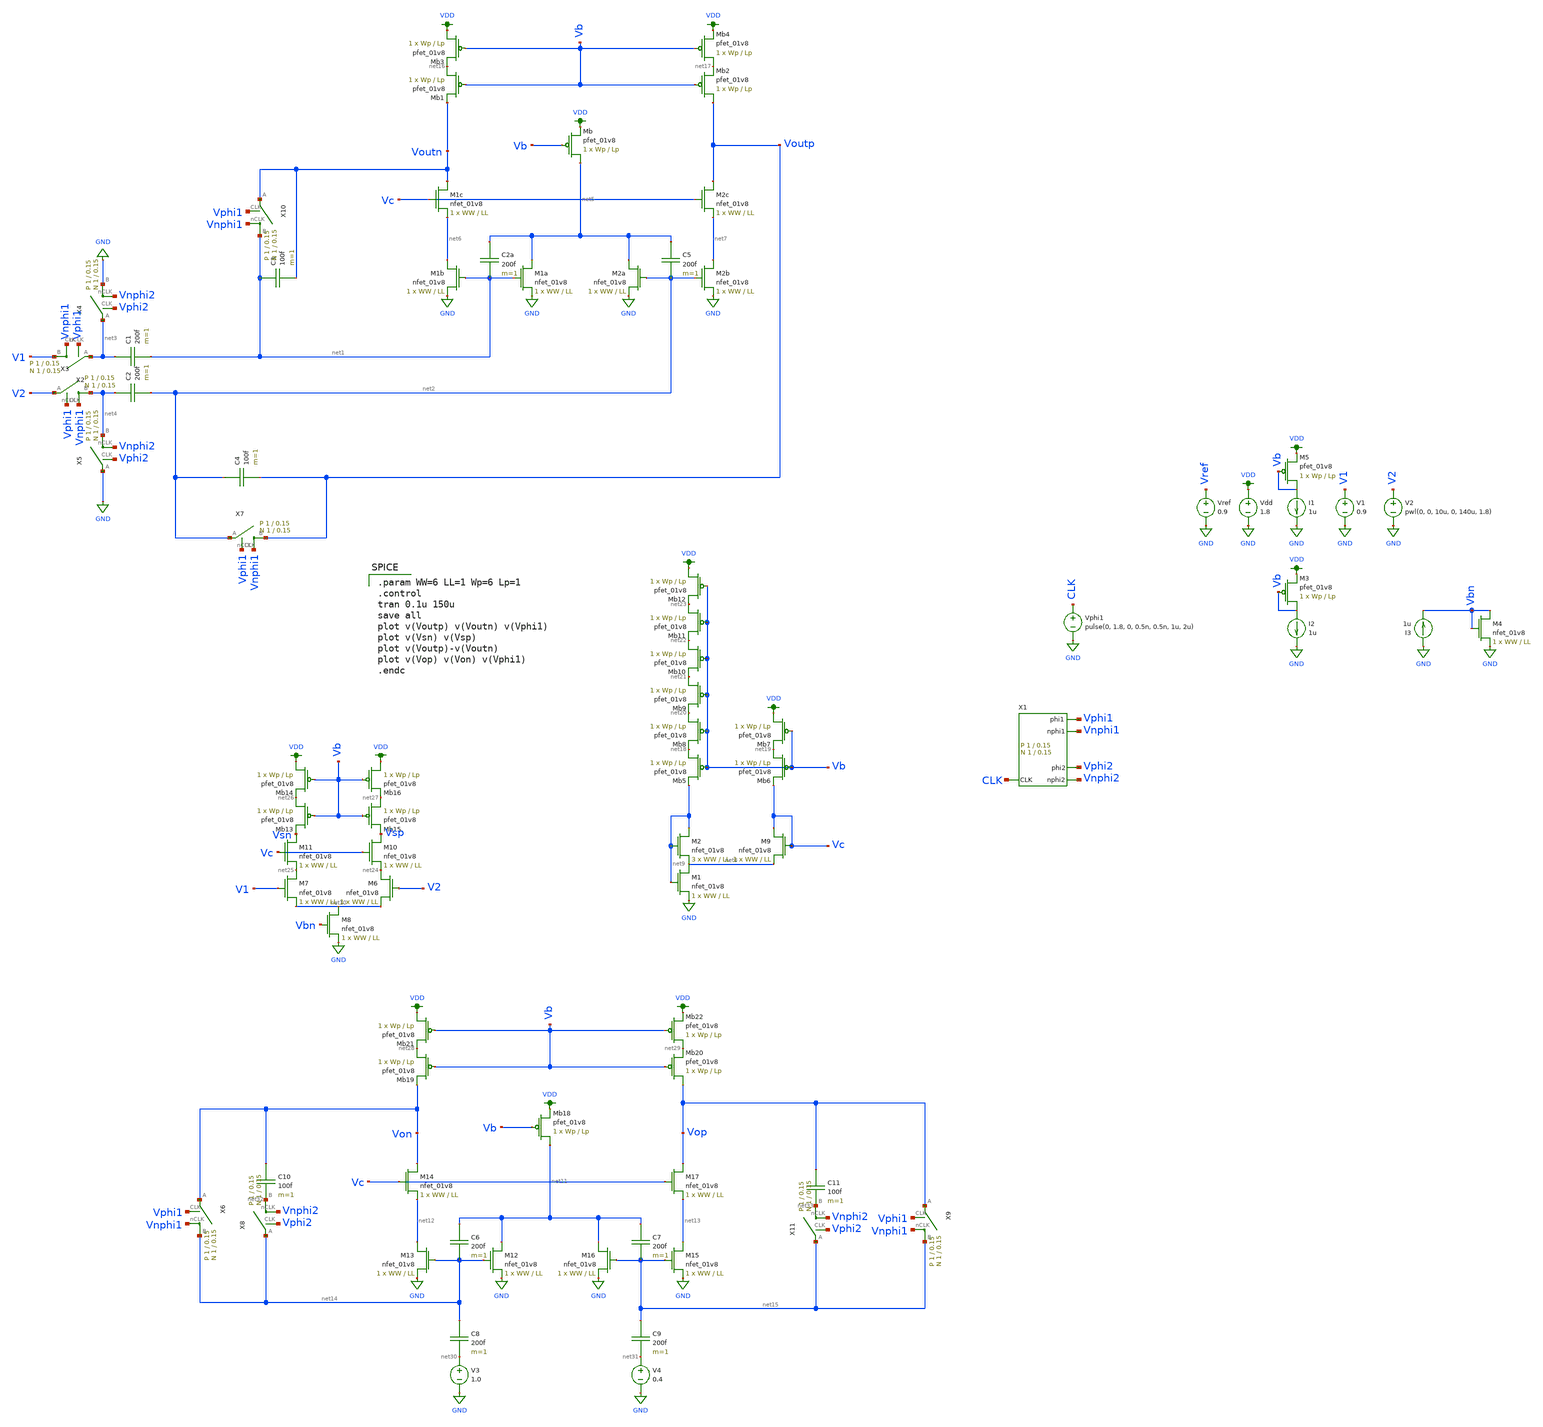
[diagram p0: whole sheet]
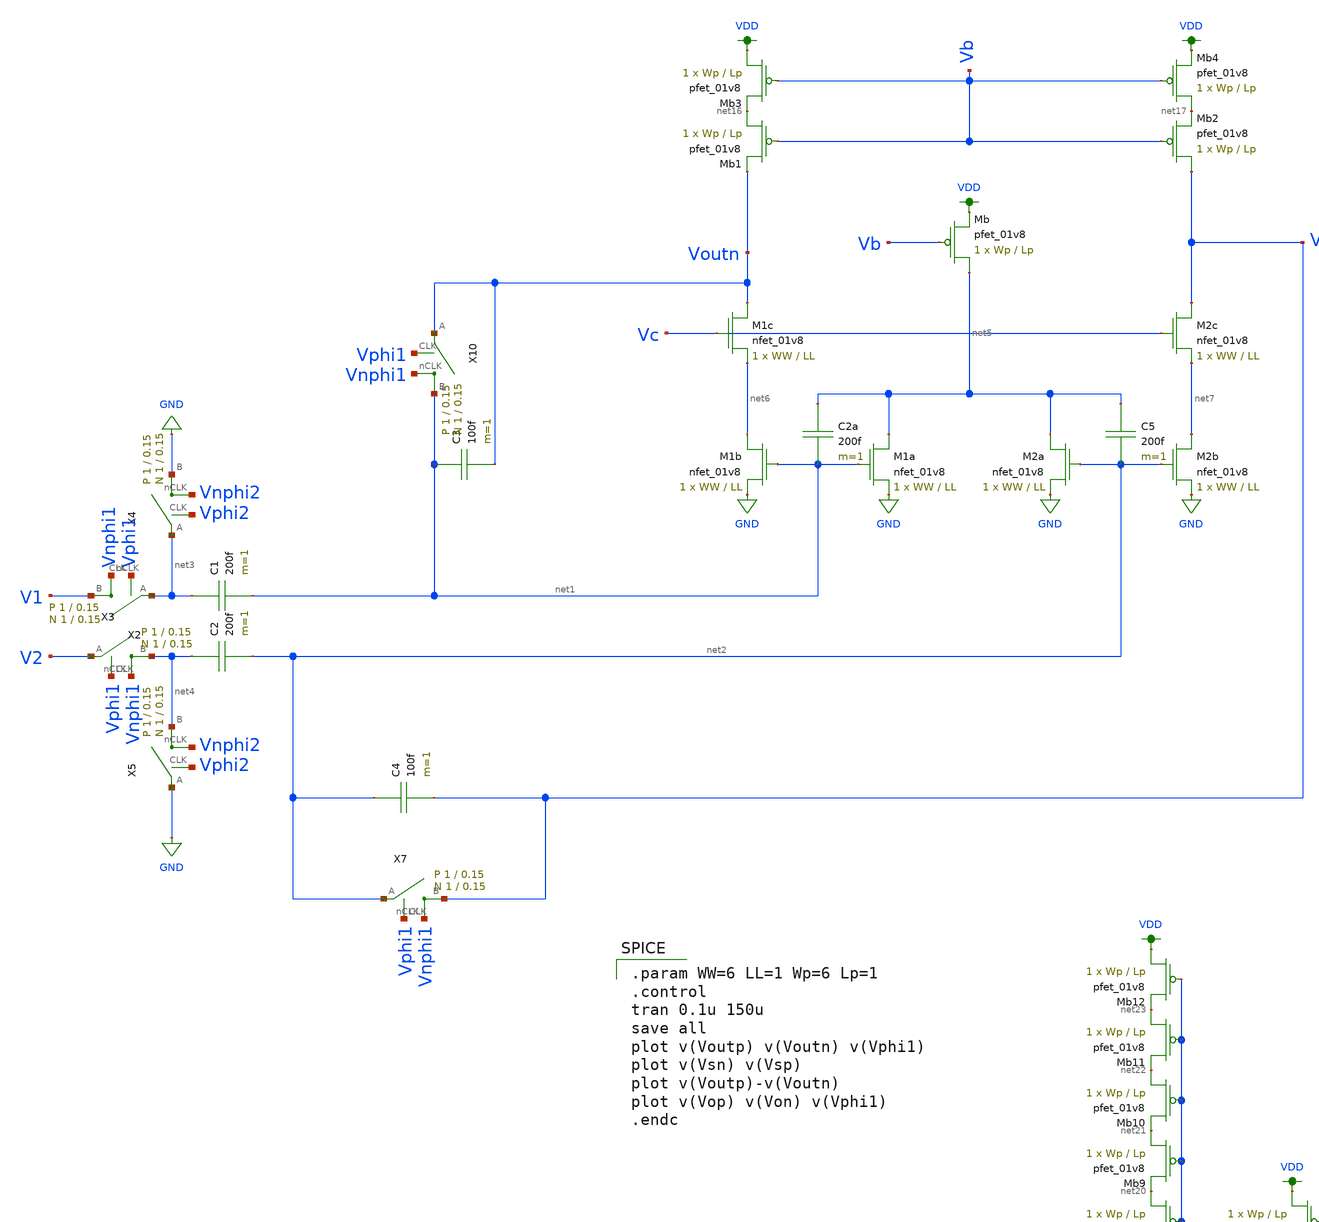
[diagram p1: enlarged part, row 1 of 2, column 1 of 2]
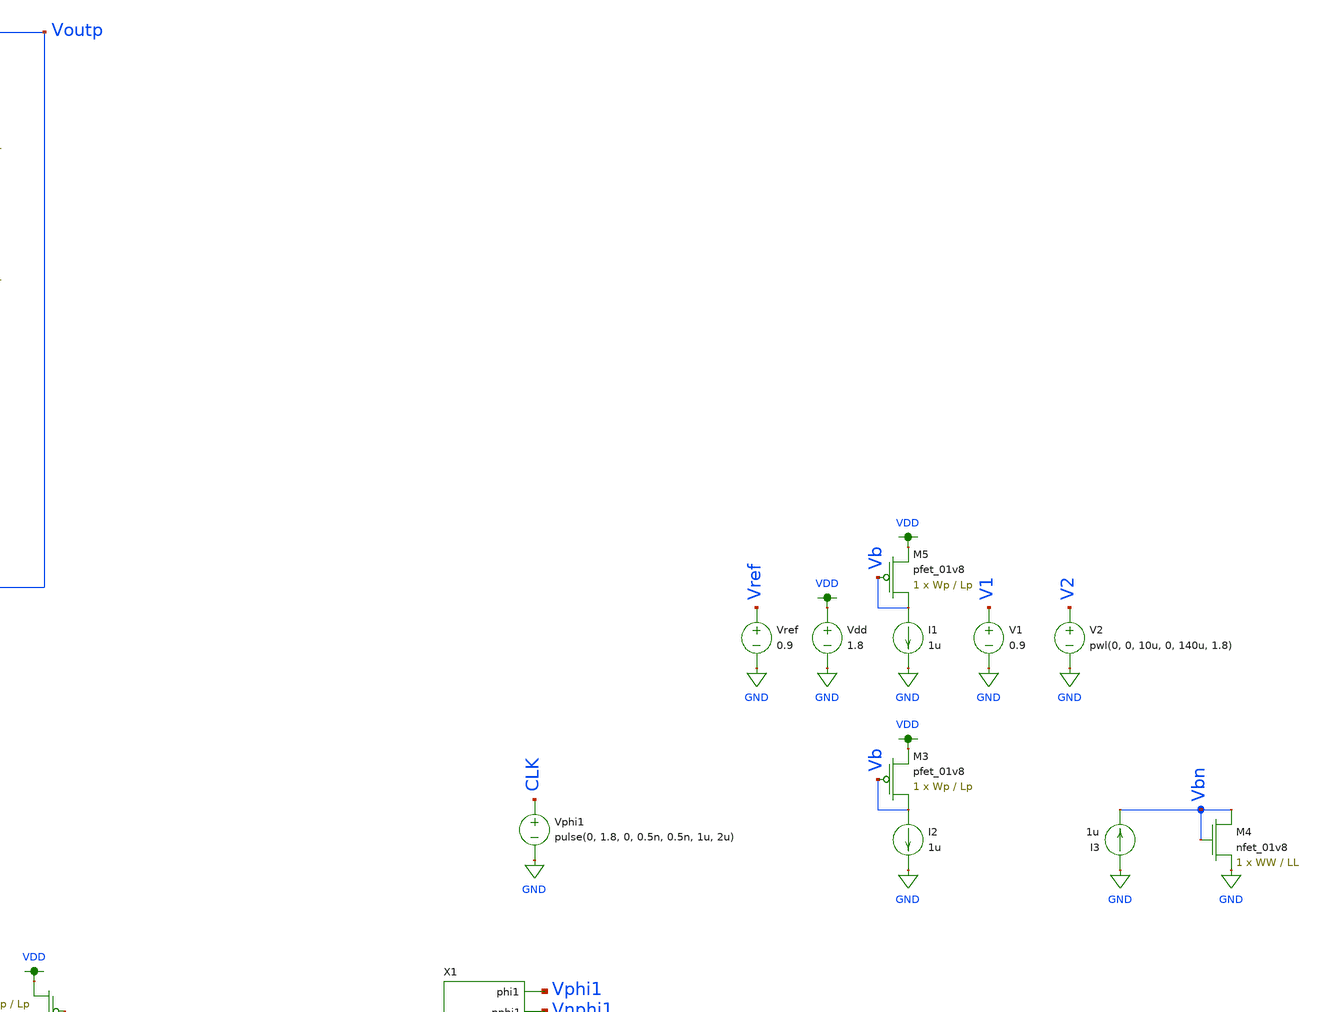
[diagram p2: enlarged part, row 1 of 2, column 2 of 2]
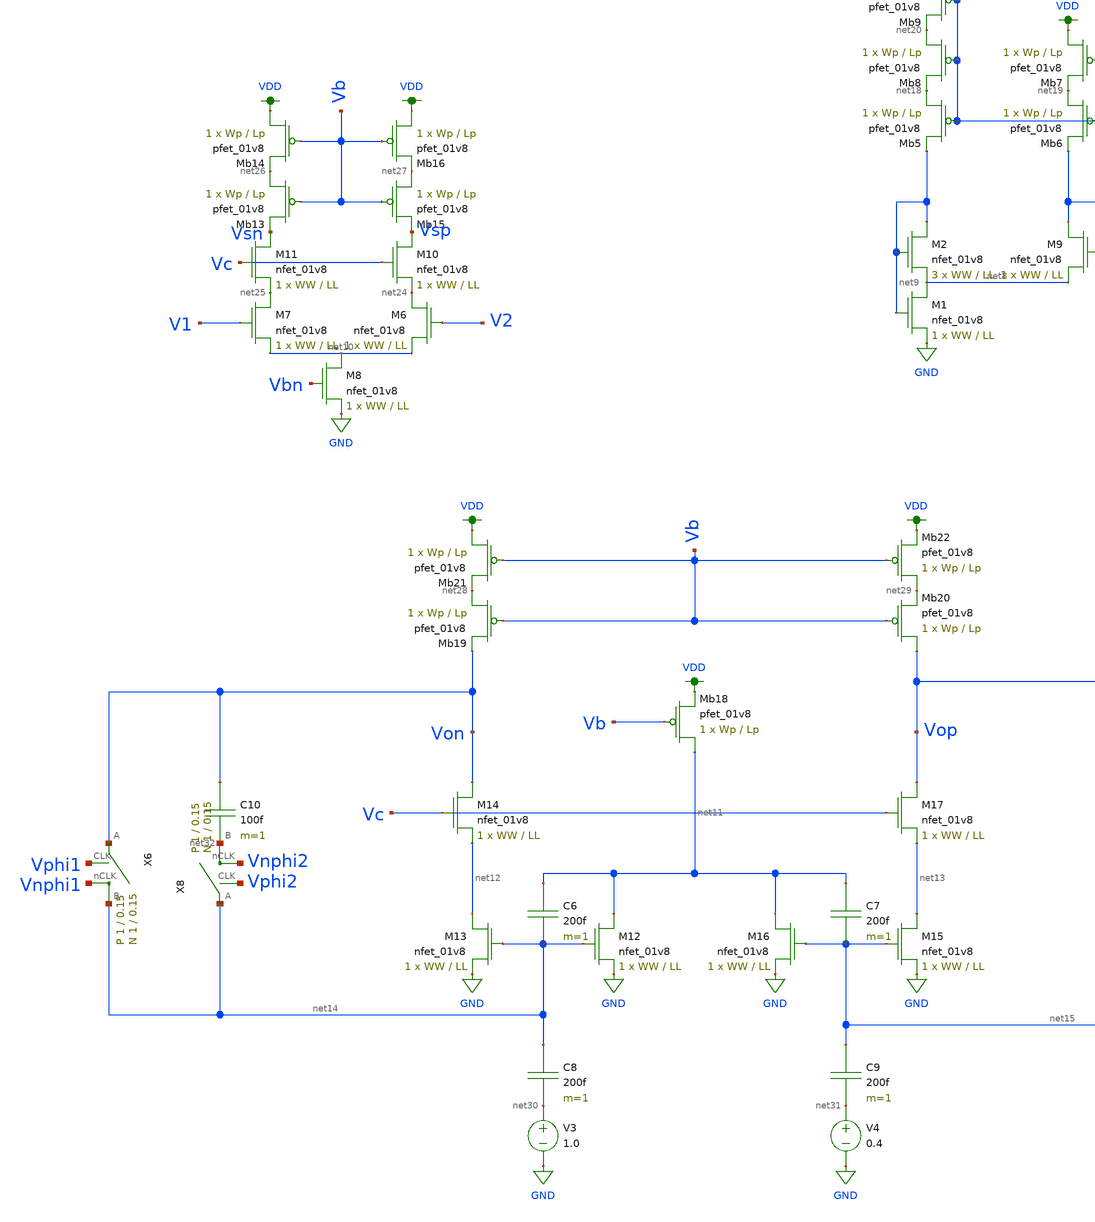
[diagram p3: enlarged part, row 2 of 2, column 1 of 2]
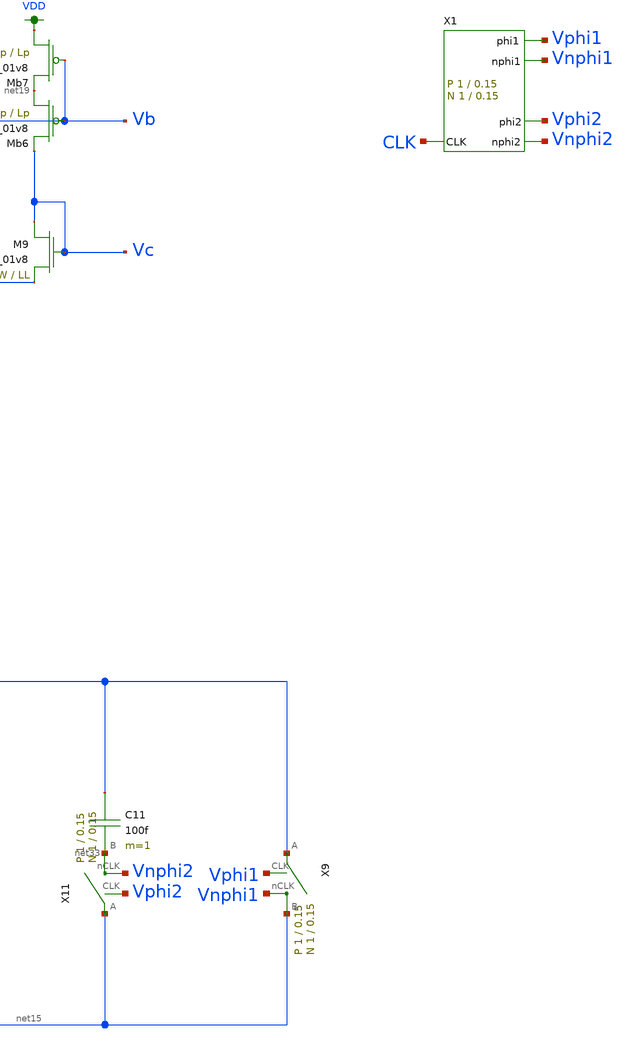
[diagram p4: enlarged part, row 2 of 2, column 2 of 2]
** sch_path: schematic/test/alpha_amp_FD.sch
**.subckt alpha_amp_FD
X2 V1 net3 Vphi1 Vnphi1 switch Wp=1 Lp=0.15 WW=1 LL=0.15
X3 net4 V2 Vphi1 Vnphi1 switch Wp=1 Lp=0.15 WW=1 LL=0.15
X4 GND net3 Vphi2 Vnphi2 switch Wp=1 Lp=0.15 WW=1 LL=0.15
X5 net4 GND Vphi2 Vnphi2 switch Wp=1 Lp=0.15 WW=1 LL=0.15
X7 Voutp net2 Vphi1 Vnphi1 switch Wp=1 Lp=0.15 WW=1 LL=0.15
Vdd VDD GND 1.8
V1 V1 GND 0.9
V2 V2 GND pwl(0, 0, 10u, 0, 140u, 1.8)
Vphi1 CLK GND pulse(0, 1.8, 0, 0.5n, 0.5n, 1u, 2u)
Vref Vref GND 0.9
XM1a net5 net1 GND GND sky130_fd_pr__nfet_01v8 L=LL W=WW nf=1 ad='int((nf+1)/2) * W/nf * 0.29' as='int((nf+2)/2) * W/nf * 0.29'
+ pd='2*int((nf+1)/2) * (W/nf + 0.29)' ps='2*int((nf+2)/2) * (W/nf + 0.29)' nrd='0.29 / W' nrs='0.29 / W'
+ sa=0 sb=0 sd=0 mult=1 m=1
XM1b net6 net1 GND GND sky130_fd_pr__nfet_01v8 L=LL W=WW nf=1 ad='int((nf+1)/2) * W/nf * 0.29' as='int((nf+2)/2) * W/nf * 0.29'
+ pd='2*int((nf+1)/2) * (W/nf + 0.29)' ps='2*int((nf+2)/2) * (W/nf + 0.29)' nrd='0.29 / W' nrs='0.29 / W'
+ sa=0 sb=0 sd=0 mult=1 m=1
XM1c Voutn Vc net6 GND sky130_fd_pr__nfet_01v8 L=LL W=WW nf=1 ad='int((nf+1)/2) * W/nf * 0.29' as='int((nf+2)/2) * W/nf * 0.29'
+ pd='2*int((nf+1)/2) * (W/nf + 0.29)' ps='2*int((nf+2)/2) * (W/nf + 0.29)' nrd='0.29 / W' nrs='0.29 / W'
+ sa=0 sb=0 sd=0 mult=1 m=1
XM2b net7 net2 GND GND sky130_fd_pr__nfet_01v8 L=LL W=WW nf=1 ad='int((nf+1)/2) * W/nf * 0.29' as='int((nf+2)/2) * W/nf * 0.29'
+ pd='2*int((nf+1)/2) * (W/nf + 0.29)' ps='2*int((nf+2)/2) * (W/nf + 0.29)' nrd='0.29 / W' nrs='0.29 / W'
+ sa=0 sb=0 sd=0 mult=1 m=1
XM2a net5 net2 GND GND sky130_fd_pr__nfet_01v8 L=LL W=WW nf=1 ad='int((nf+1)/2) * W/nf * 0.29' as='int((nf+2)/2) * W/nf * 0.29'
+ pd='2*int((nf+1)/2) * (W/nf + 0.29)' ps='2*int((nf+2)/2) * (W/nf + 0.29)' nrd='0.29 / W' nrs='0.29 / W'
+ sa=0 sb=0 sd=0 mult=1 m=1
XM2c Voutp Vc net7 GND sky130_fd_pr__nfet_01v8 L=LL W=WW nf=1 ad='int((nf+1)/2) * W/nf * 0.29' as='int((nf+2)/2) * W/nf * 0.29'
+ pd='2*int((nf+1)/2) * (W/nf + 0.29)' ps='2*int((nf+2)/2) * (W/nf + 0.29)' nrd='0.29 / W' nrs='0.29 / W'
+ sa=0 sb=0 sd=0 mult=1 m=1
XMb net5 Vb VDD VDD sky130_fd_pr__pfet_01v8 L=Lp W=Wp nf=1 ad='int((nf+1)/2) * W/nf * 0.29' as='int((nf+2)/2) * W/nf * 0.29'
+ pd='2*int((nf+1)/2) * (W/nf + 0.29)' ps='2*int((nf+2)/2) * (W/nf + 0.29)' nrd='0.29 / W' nrs='0.29 / W'
+ sa=0 sb=0 sd=0 mult=1 m=1
C2a net5 net1 200f m=1
XMb1 net16 Vb Voutn VDD sky130_fd_pr__pfet_01v8 L=Lp W=Wp nf=1 ad='int((nf+1)/2) * W/nf * 0.29' as='int((nf+2)/2) * W/nf * 0.29'
+ pd='2*int((nf+1)/2) * (W/nf + 0.29)' ps='2*int((nf+2)/2) * (W/nf + 0.29)' nrd='0.29 / W' nrs='0.29 / W'
+ sa=0 sb=0 sd=0 mult=1 m=1
XM5 Vb Vb VDD VDD sky130_fd_pr__pfet_01v8 L=Lp W=Wp nf=1 ad='int((nf+1)/2) * W/nf * 0.29' as='int((nf+2)/2) * W/nf * 0.29'
+ pd='2*int((nf+1)/2) * (W/nf + 0.29)' ps='2*int((nf+2)/2) * (W/nf + 0.29)' nrd='0.29 / W' nrs='0.29 / W'
+ sa=0 sb=0 sd=0 mult=1 m=1
I1 Vb GND 1u
XMb2 Voutp Vb net17 VDD sky130_fd_pr__pfet_01v8 L=Lp W=Wp nf=1 ad='int((nf+1)/2) * W/nf * 0.29' as='int((nf+2)/2) * W/nf * 0.29'
+ pd='2*int((nf+1)/2) * (W/nf + 0.29)' ps='2*int((nf+2)/2) * (W/nf + 0.29)' nrd='0.29 / W' nrs='0.29 / W'
+ sa=0 sb=0 sd=0 mult=1 m=1
X1 Vphi1 Vphi2 CLK Vnphi1 Vnphi2 clk_gen Wp=1 Lp=0.15 WW=1 LL=0.15
XMb3 VDD Vb net16 VDD sky130_fd_pr__pfet_01v8 L=Lp W=Wp nf=1 ad='int((nf+1)/2) * W/nf * 0.29' as='int((nf+2)/2) * W/nf * 0.29'
+ pd='2*int((nf+1)/2) * (W/nf + 0.29)' ps='2*int((nf+2)/2) * (W/nf + 0.29)' nrd='0.29 / W' nrs='0.29 / W'
+ sa=0 sb=0 sd=0 mult=1 m=1
XMb4 net17 Vb VDD VDD sky130_fd_pr__pfet_01v8 L=Lp W=Wp nf=1 ad='int((nf+1)/2) * W/nf * 0.29' as='int((nf+2)/2) * W/nf * 0.29'
+ pd='2*int((nf+1)/2) * (W/nf + 0.29)' ps='2*int((nf+2)/2) * (W/nf + 0.29)' nrd='0.29 / W' nrs='0.29 / W'
+ sa=0 sb=0 sd=0 mult=1 m=1
XM1 net8 net9 GND GND sky130_fd_pr__nfet_01v8 L=LL W=WW nf=1 ad='int((nf+1)/2) * W/nf * 0.29' as='int((nf+2)/2) * W/nf * 0.29'
+ pd='2*int((nf+1)/2) * (W/nf + 0.29)' ps='2*int((nf+2)/2) * (W/nf + 0.29)' nrd='0.29 / W' nrs='0.29 / W'
+ sa=0 sb=0 sd=0 mult=1 m=1
XM2 net9 net9 net8 GND sky130_fd_pr__nfet_01v8 L=LL W=WW nf=1 ad='int((nf+1)/2) * W/nf * 0.29' as='int((nf+2)/2) * W/nf * 0.29'
+ pd='2*int((nf+1)/2) * (W/nf + 0.29)' ps='2*int((nf+2)/2) * (W/nf + 0.29)' nrd='0.29 / W' nrs='0.29 / W'
+ sa=0 sb=0 sd=0 mult=3 m=3
XM9 Vc Vc net8 GND sky130_fd_pr__nfet_01v8 L=LL W=WW nf=1 ad='int((nf+1)/2) * W/nf * 0.29' as='int((nf+2)/2) * W/nf * 0.29'
+ pd='2*int((nf+1)/2) * (W/nf + 0.29)' ps='2*int((nf+2)/2) * (W/nf + 0.29)' nrd='0.29 / W' nrs='0.29 / W'
+ sa=0 sb=0 sd=0 mult=1 m=1
XMb5 net18 Vb net9 VDD sky130_fd_pr__pfet_01v8 L=Lp W=Wp nf=1 ad='int((nf+1)/2) * W/nf * 0.29' as='int((nf+2)/2) * W/nf * 0.29'
+ pd='2*int((nf+1)/2) * (W/nf + 0.29)' ps='2*int((nf+2)/2) * (W/nf + 0.29)' nrd='0.29 / W' nrs='0.29 / W'
+ sa=0 sb=0 sd=0 mult=1 m=1
XMb6 net19 Vb Vc VDD sky130_fd_pr__pfet_01v8 L=Lp W=Wp nf=1 ad='int((nf+1)/2) * W/nf * 0.29' as='int((nf+2)/2) * W/nf * 0.29'
+ pd='2*int((nf+1)/2) * (W/nf + 0.29)' ps='2*int((nf+2)/2) * (W/nf + 0.29)' nrd='0.29 / W' nrs='0.29 / W'
+ sa=0 sb=0 sd=0 mult=1 m=1
XMb7 VDD Vb net19 VDD sky130_fd_pr__pfet_01v8 L=Lp W=Wp nf=1 ad='int((nf+1)/2) * W/nf * 0.29' as='int((nf+2)/2) * W/nf * 0.29'
+ pd='2*int((nf+1)/2) * (W/nf + 0.29)' ps='2*int((nf+2)/2) * (W/nf + 0.29)' nrd='0.29 / W' nrs='0.29 / W'
+ sa=0 sb=0 sd=0 mult=1 m=1
XMb8 net20 Vb net18 VDD sky130_fd_pr__pfet_01v8 L=Lp W=Wp nf=1 ad='int((nf+1)/2) * W/nf * 0.29' as='int((nf+2)/2) * W/nf * 0.29'
+ pd='2*int((nf+1)/2) * (W/nf + 0.29)' ps='2*int((nf+2)/2) * (W/nf + 0.29)' nrd='0.29 / W' nrs='0.29 / W'
+ sa=0 sb=0 sd=0 mult=1 m=1
XMb9 net21 Vb net20 VDD sky130_fd_pr__pfet_01v8 L=Lp W=Wp nf=1 ad='int((nf+1)/2) * W/nf * 0.29' as='int((nf+2)/2) * W/nf * 0.29'
+ pd='2*int((nf+1)/2) * (W/nf + 0.29)' ps='2*int((nf+2)/2) * (W/nf + 0.29)' nrd='0.29 / W' nrs='0.29 / W'
+ sa=0 sb=0 sd=0 mult=1 m=1
XMb10 net22 Vb net21 VDD sky130_fd_pr__pfet_01v8 L=Lp W=Wp nf=1 ad='int((nf+1)/2) * W/nf * 0.29' as='int((nf+2)/2) * W/nf * 0.29'
+ pd='2*int((nf+1)/2) * (W/nf + 0.29)' ps='2*int((nf+2)/2) * (W/nf + 0.29)' nrd='0.29 / W' nrs='0.29 / W'
+ sa=0 sb=0 sd=0 mult=1 m=1
XMb11 net23 Vb net22 VDD sky130_fd_pr__pfet_01v8 L=Lp W=Wp nf=1 ad='int((nf+1)/2) * W/nf * 0.29' as='int((nf+2)/2) * W/nf * 0.29'
+ pd='2*int((nf+1)/2) * (W/nf + 0.29)' ps='2*int((nf+2)/2) * (W/nf + 0.29)' nrd='0.29 / W' nrs='0.29 / W'
+ sa=0 sb=0 sd=0 mult=1 m=1
XMb12 VDD Vb net23 VDD sky130_fd_pr__pfet_01v8 L=Lp W=Wp nf=1 ad='int((nf+1)/2) * W/nf * 0.29' as='int((nf+2)/2) * W/nf * 0.29'
+ pd='2*int((nf+1)/2) * (W/nf + 0.29)' ps='2*int((nf+2)/2) * (W/nf + 0.29)' nrd='0.29 / W' nrs='0.29 / W'
+ sa=0 sb=0 sd=0 mult=1 m=1
C5 net5 net2 200f m=1
C3 net1 Voutn 100f m=1
C1 net3 net1 200f m=1
C2 net4 net2 200f m=1
C4 net2 Voutp 100f m=1
X10 net1 Voutn Vphi1 Vnphi1 switch Wp=1 Lp=0.15 WW=1 LL=0.15
XM3 Vb Vb VDD VDD sky130_fd_pr__pfet_01v8 L=Lp W=Wp nf=1 ad='int((nf+1)/2) * W/nf * 0.29' as='int((nf+2)/2) * W/nf * 0.29'
+ pd='2*int((nf+1)/2) * (W/nf + 0.29)' ps='2*int((nf+2)/2) * (W/nf + 0.29)' nrd='0.29 / W' nrs='0.29 / W'
+ sa=0 sb=0 sd=0 mult=1 m=1
I2 Vb GND 1u
I3 GND Vbn 1u
XM4 Vbn Vbn GND GND sky130_fd_pr__nfet_01v8 L=LL W=WW nf=1 ad='int((nf+1)/2) * W/nf * 0.29' as='int((nf+2)/2) * W/nf * 0.29'
+ pd='2*int((nf+1)/2) * (W/nf + 0.29)' ps='2*int((nf+2)/2) * (W/nf + 0.29)' nrd='0.29 / W' nrs='0.29 / W'
+ sa=0 sb=0 sd=0 mult=1 m=1
XM6 net24 V2 net10 GND sky130_fd_pr__nfet_01v8 L=LL W=WW nf=1 ad='int((nf+1)/2) * W/nf * 0.29' as='int((nf+2)/2) * W/nf * 0.29'
+ pd='2*int((nf+1)/2) * (W/nf + 0.29)' ps='2*int((nf+2)/2) * (W/nf + 0.29)' nrd='0.29 / W' nrs='0.29 / W'
+ sa=0 sb=0 sd=0 mult=1 m=1
XM7 net25 V1 net10 GND sky130_fd_pr__nfet_01v8 L=LL W=WW nf=1 ad='int((nf+1)/2) * W/nf * 0.29' as='int((nf+2)/2) * W/nf * 0.29'
+ pd='2*int((nf+1)/2) * (W/nf + 0.29)' ps='2*int((nf+2)/2) * (W/nf + 0.29)' nrd='0.29 / W' nrs='0.29 / W'
+ sa=0 sb=0 sd=0 mult=1 m=1
XM8 net10 Vbn GND GND sky130_fd_pr__nfet_01v8 L=LL W=WW nf=1 ad='int((nf+1)/2) * W/nf * 0.29' as='int((nf+2)/2) * W/nf * 0.29'
+ pd='2*int((nf+1)/2) * (W/nf + 0.29)' ps='2*int((nf+2)/2) * (W/nf + 0.29)' nrd='0.29 / W' nrs='0.29 / W'
+ sa=0 sb=0 sd=0 mult=1 m=1
XMb13 net26 Vb Vsn VDD sky130_fd_pr__pfet_01v8 L=Lp W=Wp nf=1 ad='int((nf+1)/2) * W/nf * 0.29' as='int((nf+2)/2) * W/nf * 0.29'
+ pd='2*int((nf+1)/2) * (W/nf + 0.29)' ps='2*int((nf+2)/2) * (W/nf + 0.29)' nrd='0.29 / W' nrs='0.29 / W'
+ sa=0 sb=0 sd=0 mult=1 m=1
XMb14 VDD Vb net26 VDD sky130_fd_pr__pfet_01v8 L=Lp W=Wp nf=1 ad='int((nf+1)/2) * W/nf * 0.29' as='int((nf+2)/2) * W/nf * 0.29'
+ pd='2*int((nf+1)/2) * (W/nf + 0.29)' ps='2*int((nf+2)/2) * (W/nf + 0.29)' nrd='0.29 / W' nrs='0.29 / W'
+ sa=0 sb=0 sd=0 mult=1 m=1
XMb15 net27 Vb Vsp VDD sky130_fd_pr__pfet_01v8 L=Lp W=Wp nf=1 ad='int((nf+1)/2) * W/nf * 0.29' as='int((nf+2)/2) * W/nf * 0.29'
+ pd='2*int((nf+1)/2) * (W/nf + 0.29)' ps='2*int((nf+2)/2) * (W/nf + 0.29)' nrd='0.29 / W' nrs='0.29 / W'
+ sa=0 sb=0 sd=0 mult=1 m=1
XMb16 VDD Vb net27 VDD sky130_fd_pr__pfet_01v8 L=Lp W=Wp nf=1 ad='int((nf+1)/2) * W/nf * 0.29' as='int((nf+2)/2) * W/nf * 0.29'
+ pd='2*int((nf+1)/2) * (W/nf + 0.29)' ps='2*int((nf+2)/2) * (W/nf + 0.29)' nrd='0.29 / W' nrs='0.29 / W'
+ sa=0 sb=0 sd=0 mult=1 m=1
XM10 Vsp Vc net24 GND sky130_fd_pr__nfet_01v8 L=LL W=WW nf=1 ad='int((nf+1)/2) * W/nf * 0.29' as='int((nf+2)/2) * W/nf * 0.29'
+ pd='2*int((nf+1)/2) * (W/nf + 0.29)' ps='2*int((nf+2)/2) * (W/nf + 0.29)' nrd='0.29 / W' nrs='0.29 / W'
+ sa=0 sb=0 sd=0 mult=1 m=1
XM11 Vsn Vc net25 GND sky130_fd_pr__nfet_01v8 L=LL W=WW nf=1 ad='int((nf+1)/2) * W/nf * 0.29' as='int((nf+2)/2) * W/nf * 0.29'
+ pd='2*int((nf+1)/2) * (W/nf + 0.29)' ps='2*int((nf+2)/2) * (W/nf + 0.29)' nrd='0.29 / W' nrs='0.29 / W'
+ sa=0 sb=0 sd=0 mult=1 m=1
XM12 net11 net14 GND GND sky130_fd_pr__nfet_01v8 L=LL W=WW nf=1 ad='int((nf+1)/2) * W/nf * 0.29' as='int((nf+2)/2) * W/nf * 0.29'
+ pd='2*int((nf+1)/2) * (W/nf + 0.29)' ps='2*int((nf+2)/2) * (W/nf + 0.29)' nrd='0.29 / W' nrs='0.29 / W'
+ sa=0 sb=0 sd=0 mult=1 m=1
XM13 net12 net14 GND GND sky130_fd_pr__nfet_01v8 L=LL W=WW nf=1 ad='int((nf+1)/2) * W/nf * 0.29' as='int((nf+2)/2) * W/nf * 0.29'
+ pd='2*int((nf+1)/2) * (W/nf + 0.29)' ps='2*int((nf+2)/2) * (W/nf + 0.29)' nrd='0.29 / W' nrs='0.29 / W'
+ sa=0 sb=0 sd=0 mult=1 m=1
XM14 Von Vc net12 GND sky130_fd_pr__nfet_01v8 L=LL W=WW nf=1 ad='int((nf+1)/2) * W/nf * 0.29' as='int((nf+2)/2) * W/nf * 0.29'
+ pd='2*int((nf+1)/2) * (W/nf + 0.29)' ps='2*int((nf+2)/2) * (W/nf + 0.29)' nrd='0.29 / W' nrs='0.29 / W'
+ sa=0 sb=0 sd=0 mult=1 m=1
XM15 net13 net15 GND GND sky130_fd_pr__nfet_01v8 L=LL W=WW nf=1 ad='int((nf+1)/2) * W/nf * 0.29' as='int((nf+2)/2) * W/nf * 0.29'
+ pd='2*int((nf+1)/2) * (W/nf + 0.29)' ps='2*int((nf+2)/2) * (W/nf + 0.29)' nrd='0.29 / W' nrs='0.29 / W'
+ sa=0 sb=0 sd=0 mult=1 m=1
XM16 net11 net15 GND GND sky130_fd_pr__nfet_01v8 L=LL W=WW nf=1 ad='int((nf+1)/2) * W/nf * 0.29' as='int((nf+2)/2) * W/nf * 0.29'
+ pd='2*int((nf+1)/2) * (W/nf + 0.29)' ps='2*int((nf+2)/2) * (W/nf + 0.29)' nrd='0.29 / W' nrs='0.29 / W'
+ sa=0 sb=0 sd=0 mult=1 m=1
XM17 Vop Vc net13 GND sky130_fd_pr__nfet_01v8 L=LL W=WW nf=1 ad='int((nf+1)/2) * W/nf * 0.29' as='int((nf+2)/2) * W/nf * 0.29'
+ pd='2*int((nf+1)/2) * (W/nf + 0.29)' ps='2*int((nf+2)/2) * (W/nf + 0.29)' nrd='0.29 / W' nrs='0.29 / W'
+ sa=0 sb=0 sd=0 mult=1 m=1
XMb18 net11 Vb VDD VDD sky130_fd_pr__pfet_01v8 L=Lp W=Wp nf=1 ad='int((nf+1)/2) * W/nf * 0.29' as='int((nf+2)/2) * W/nf * 0.29'
+ pd='2*int((nf+1)/2) * (W/nf + 0.29)' ps='2*int((nf+2)/2) * (W/nf + 0.29)' nrd='0.29 / W' nrs='0.29 / W'
+ sa=0 sb=0 sd=0 mult=1 m=1
C6 net11 net14 200f m=1
XMb19 net28 Vb Von VDD sky130_fd_pr__pfet_01v8 L=Lp W=Wp nf=1 ad='int((nf+1)/2) * W/nf * 0.29' as='int((nf+2)/2) * W/nf * 0.29'
+ pd='2*int((nf+1)/2) * (W/nf + 0.29)' ps='2*int((nf+2)/2) * (W/nf + 0.29)' nrd='0.29 / W' nrs='0.29 / W'
+ sa=0 sb=0 sd=0 mult=1 m=1
XMb20 Vop Vb net29 VDD sky130_fd_pr__pfet_01v8 L=Lp W=Wp nf=1 ad='int((nf+1)/2) * W/nf * 0.29' as='int((nf+2)/2) * W/nf * 0.29'
+ pd='2*int((nf+1)/2) * (W/nf + 0.29)' ps='2*int((nf+2)/2) * (W/nf + 0.29)' nrd='0.29 / W' nrs='0.29 / W'
+ sa=0 sb=0 sd=0 mult=1 m=1
XMb21 VDD Vb net28 VDD sky130_fd_pr__pfet_01v8 L=Lp W=Wp nf=1 ad='int((nf+1)/2) * W/nf * 0.29' as='int((nf+2)/2) * W/nf * 0.29'
+ pd='2*int((nf+1)/2) * (W/nf + 0.29)' ps='2*int((nf+2)/2) * (W/nf + 0.29)' nrd='0.29 / W' nrs='0.29 / W'
+ sa=0 sb=0 sd=0 mult=1 m=1
XMb22 net29 Vb VDD VDD sky130_fd_pr__pfet_01v8 L=Lp W=Wp nf=1 ad='int((nf+1)/2) * W/nf * 0.29' as='int((nf+2)/2) * W/nf * 0.29'
+ pd='2*int((nf+1)/2) * (W/nf + 0.29)' ps='2*int((nf+2)/2) * (W/nf + 0.29)' nrd='0.29 / W' nrs='0.29 / W'
+ sa=0 sb=0 sd=0 mult=1 m=1
C7 net11 net15 200f m=1
C8 net14 net30 200f m=1
C9 net15 net31 200f m=1
C10 Von net32 100f m=1
C11 Vop net33 100f m=1
X6 net14 Von Vphi1 Vnphi1 switch Wp=1 Lp=0.15 WW=1 LL=0.15
X8 net32 net14 Vphi2 Vnphi2 switch Wp=1 Lp=0.15 WW=1 LL=0.15
X11 net33 net15 Vphi2 Vnphi2 switch Wp=1 Lp=0.15 WW=1 LL=0.15
X9 net15 Vop Vphi1 Vnphi1 switch Wp=1 Lp=0.15 WW=1 LL=0.15
V3 net30 GND 1.0
V4 net31 GND 0.4
**** begin user architecture code

.option wnflag=1
.param MC_SWITCH=0.0
.lib ~/skywater/skywater-pdk/libraries/sky130_fd_pr_ngspice/latest/models/sky130.lib.spice tt


.param WW=6 LL=1 Wp=6 Lp=1
.control
tran 0.1u 150u
save all
plot v(Voutp) v(Voutn) v(Vphi1)
plot v(Vsn) v(Vsp)
plot v(Voutp)-v(Voutn)
plot v(Vop) v(Von) v(Vphi1)
.endc

**** end user architecture code
**.ends
.GLOBAL GND
.GLOBAL VDD
.end
